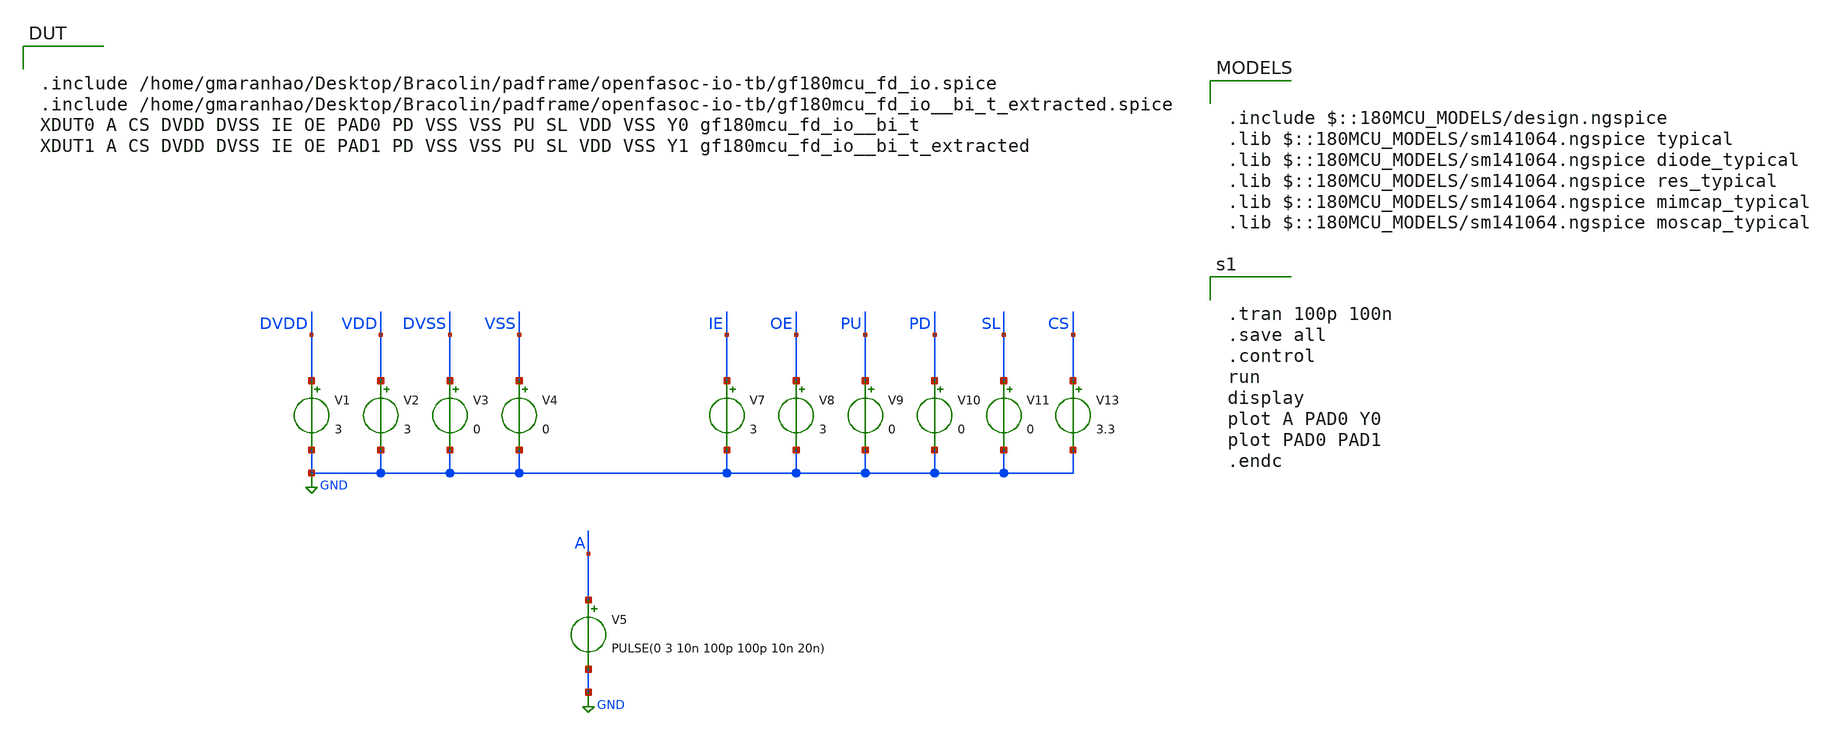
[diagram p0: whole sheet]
** sch_path: padframe/openfasoc-io-tb/digital_io_switching_pex.sch
**.subckt digital_io_switching_pex
V1 DVDD GND 3
V2 VDD GND 3
V3 DVSS GND 0
V4 VSS GND 0
V5 A GND PULSE(0 3 10n 100p 100p 10n 20n)
V7 IE GND 3
V8 OE GND 3
V9 PU GND 0
V10 PD GND 0
V11 SL GND 0
V13 CS GND 3.3
**** begin user architecture code


.tran 100p 100n
.save all
.control
run
display
plot A PAD0 Y0
plot PAD0 PAD1
.endc



.include $::180MCU_MODELS/design.ngspice
.lib $::180MCU_MODELS/sm141064.ngspice typical
.lib $::180MCU_MODELS/sm141064.ngspice diode_typical
.lib $::180MCU_MODELS/sm141064.ngspice res_typical
.lib $::180MCU_MODELS/sm141064.ngspice mimcap_typical
.lib $::180MCU_MODELS/sm141064.ngspice moscap_typical


.include /home/gmaranhao/Desktop/Bracolin/padframe/openfasoc-io-tb/gf180mcu_fd_io.spice
.include /home/gmaranhao/Desktop/Bracolin/padframe/openfasoc-io-tb/gf180mcu_fd_io__bi_t_extracted.spice
XDUT0 A CS DVDD DVSS IE OE PAD0 PD VSS VSS PU SL VDD VSS Y0 gf180mcu_fd_io__bi_t
XDUT1 A CS DVDD DVSS IE OE PAD1 PD VSS VSS PU SL VDD VSS Y1 gf180mcu_fd_io__bi_t_extracted

**** end user architecture code
**.ends
.GLOBAL GND
.end
